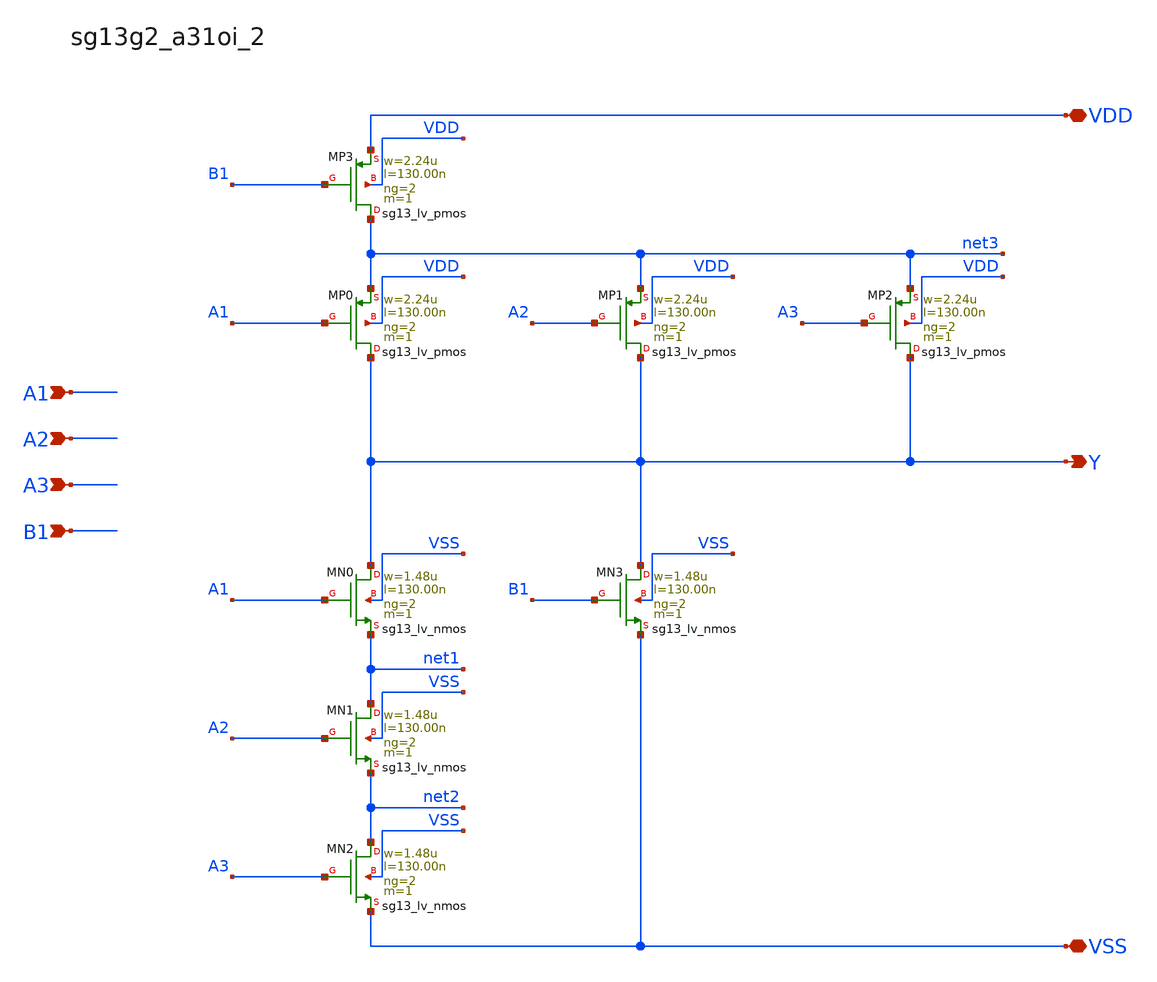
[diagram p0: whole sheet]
** sch_path: outputs/sg13g2_cells/cells/sg13g2_a31oi_2/sg13g2_a31oi_2.sch
**.subckt sg13g2_a31oi_2 Y A1 A2 A3 B1 VDD VSS
*.opin Y
*.ipin A1
*.ipin A2
*.ipin A3
*.ipin B1
*.iopin VDD
*.iopin VSS
XMN0 Y A1 net1 VSS sg13_lv_nmos w=1.48u l=130.00n ng=2 m=1 mm_ok=1
XMN1 net1 A2 net2 VSS sg13_lv_nmos w=1.48u l=130.00n ng=2 m=1 mm_ok=1
XMN2 net2 A3 VSS VSS sg13_lv_nmos w=1.48u l=130.00n ng=2 m=1 mm_ok=1
XMN3 Y B1 VSS VSS sg13_lv_nmos w=1.48u l=130.00n ng=2 m=1 mm_ok=1
XMP0 Y A1 net3 VDD sg13_lv_pmos w=2.24u l=130.00n ng=2 m=1 mm_ok=1
XMP1 Y A2 net3 VDD sg13_lv_pmos w=2.24u l=130.00n ng=2 m=1 mm_ok=1
XMP2 Y A3 net3 VDD sg13_lv_pmos w=2.24u l=130.00n ng=2 m=1 mm_ok=1
XMP3 net3 B1 VDD VDD sg13_lv_pmos w=2.24u l=130.00n ng=2 m=1 mm_ok=1
**.ends
.end
